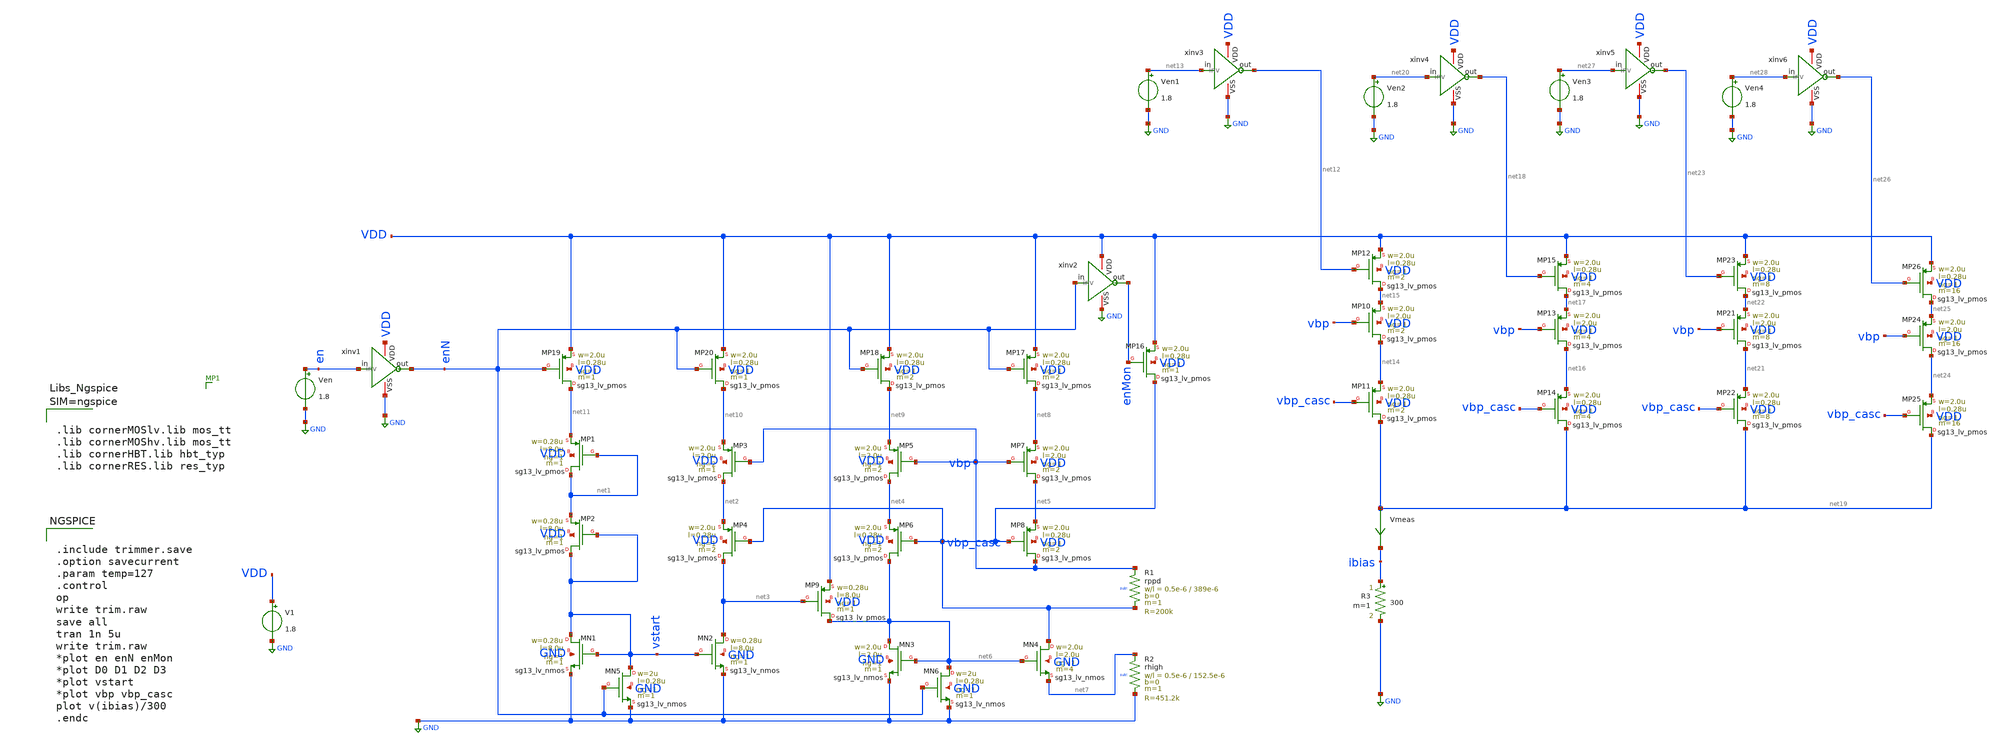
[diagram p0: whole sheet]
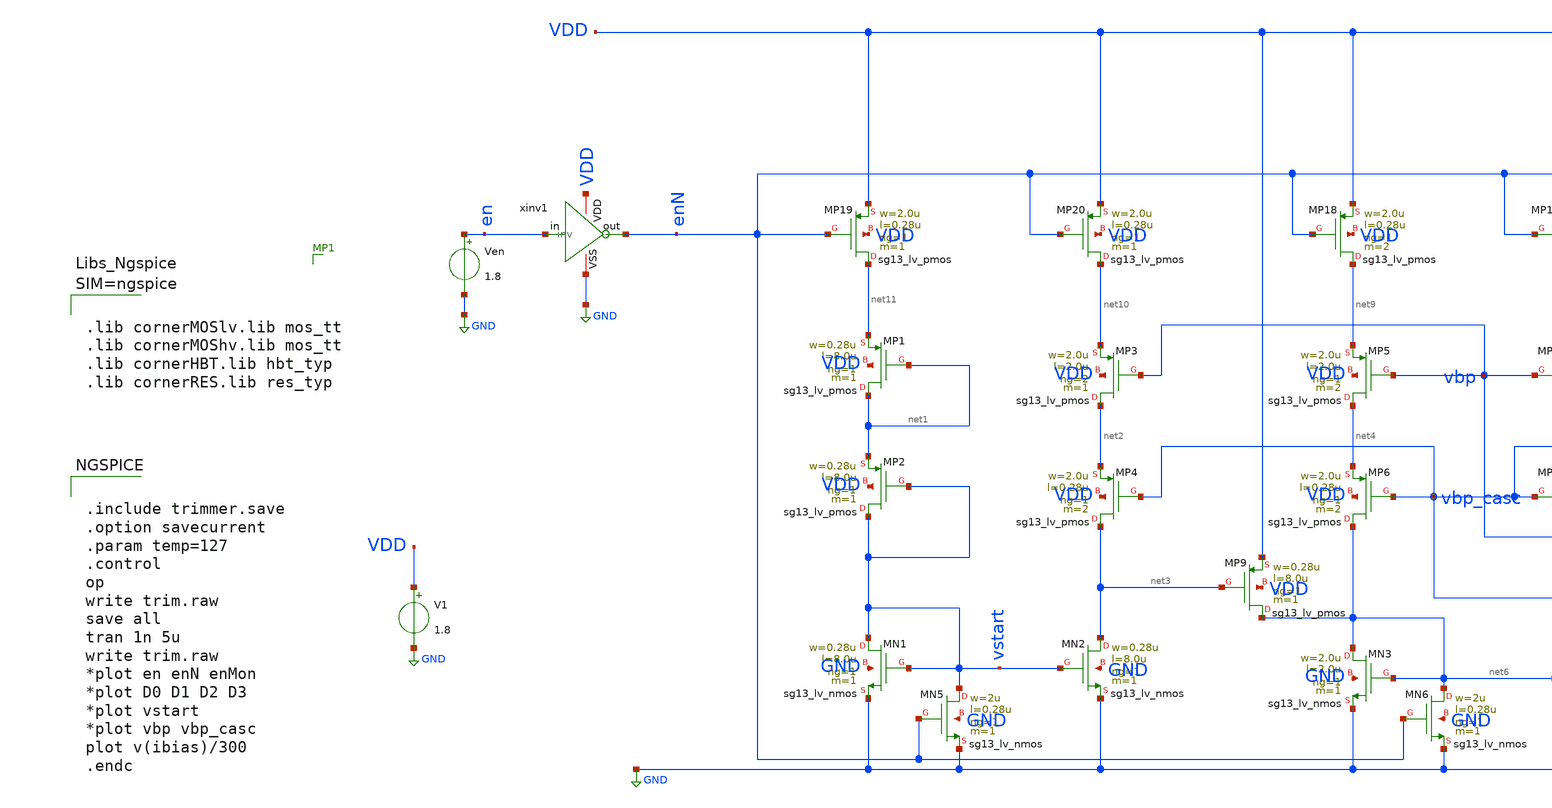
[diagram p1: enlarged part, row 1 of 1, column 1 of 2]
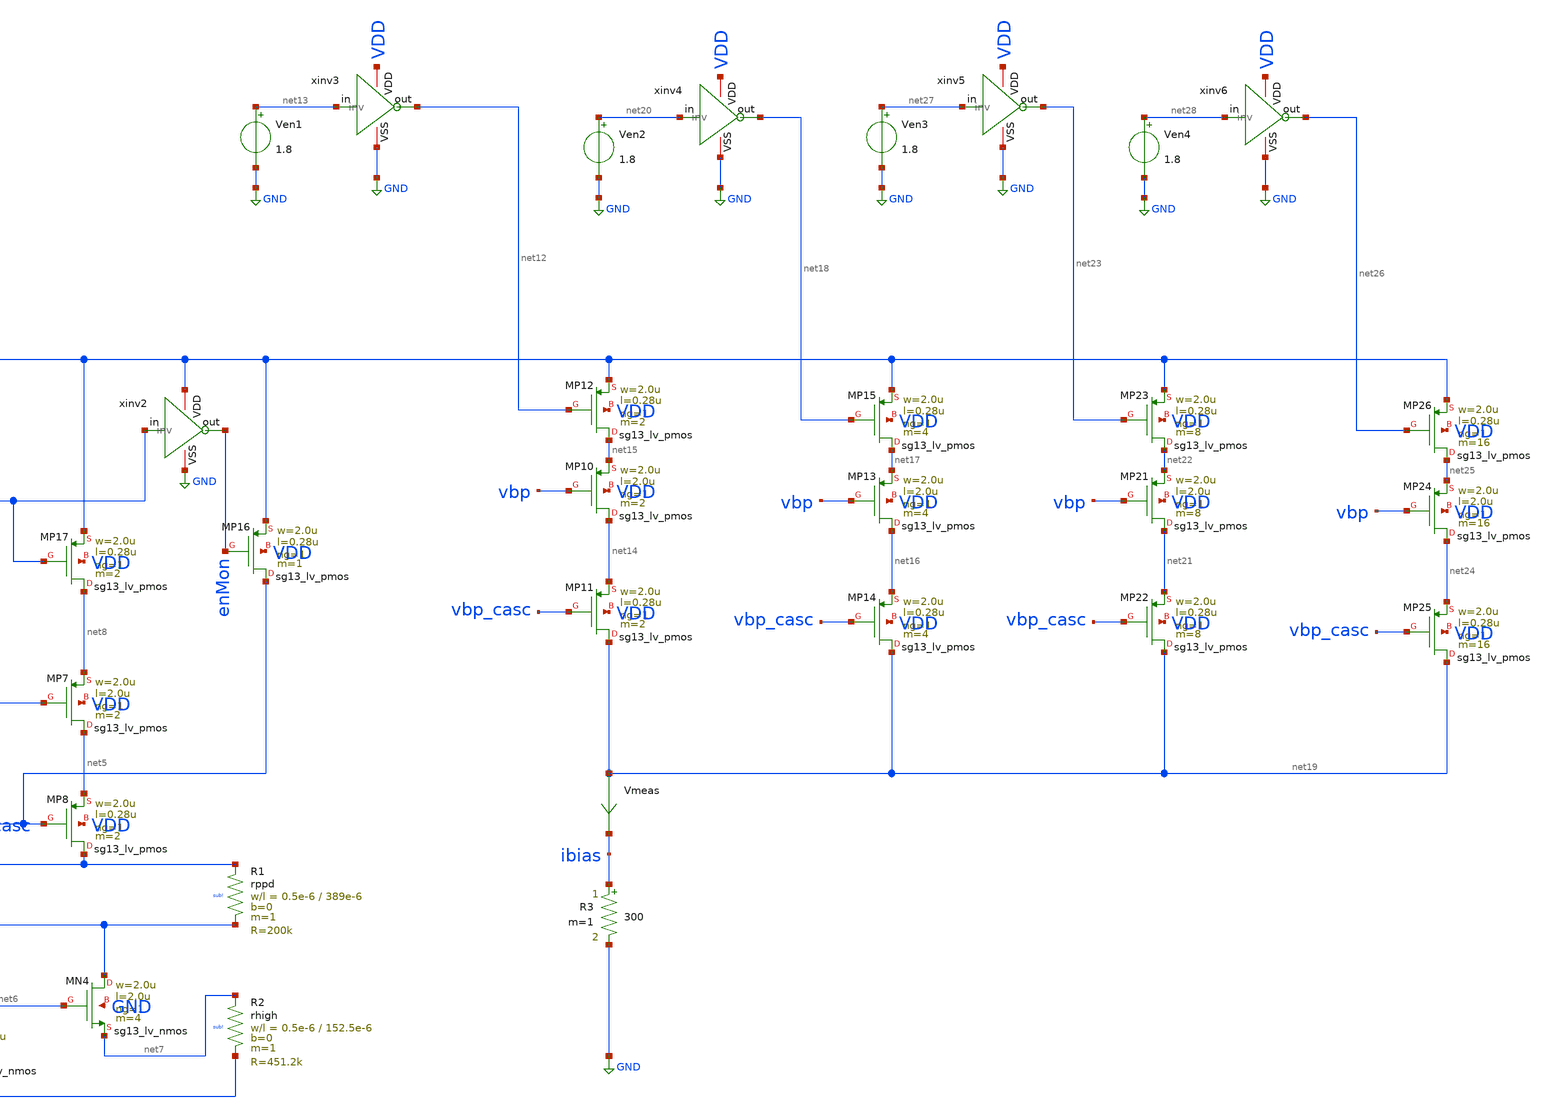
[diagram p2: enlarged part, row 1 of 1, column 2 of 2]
** sch_path: blocks/composite/dpi_adexp_neuron/design_data/xschem/dev/trimmer2_final.sch
**.subckt trimmer2_final
XMP1 net1 net1 net11 VDD sg13_lv_pmos w=0.28u l=8.0u ng=1 m=1 mm_ok=1
XMP2 vstart vstart net1 VDD sg13_lv_pmos w=0.28u l=8.0u ng=1 m=1 mm_ok=1
XMN2 net3 vstart GND GND sg13_lv_nmos w=0.28u l=8.0u ng=1 m=1 mm_ok=1
XMN1 vstart vstart GND GND sg13_lv_nmos w=0.28u l=8.0u ng=1 m=1 mm_ok=1
XMP3 net2 vbp net10 VDD sg13_lv_pmos w=2.0u l=2.0u ng=2 m=1 mm_ok=1
XMP4 net3 vbp_casc net2 VDD sg13_lv_pmos w=2.0u l=0.28u ng=1 m=2 mm_ok=1
XMP5 net4 vbp net9 VDD sg13_lv_pmos w=2.0u l=2.0u ng=1 m=2 mm_ok=1
XMP6 net6 vbp_casc net4 VDD sg13_lv_pmos w=2.0u l=0.28u ng=1 m=2 mm_ok=1
XMP7 net5 vbp net8 VDD sg13_lv_pmos w=2.0u l=2.0u ng=1 m=2 mm_ok=1
XMP8 vbp vbp_casc net5 VDD sg13_lv_pmos w=2.0u l=0.28u ng=1 m=2 mm_ok=1
XMP9 net6 net3 VDD VDD sg13_lv_pmos w=0.28u l=8.0u ng=1 m=1 mm_ok=1
XMN3 net6 net6 GND GND sg13_lv_nmos w=2.0u l=2.0u ng=1 m=1 mm_ok=1
XMN4 vbp_casc net6 net7 GND sg13_lv_nmos w=2.0u l=2.0u ng=1 m=4 mm_ok=1
XR1 vbp vbp_casc sub! rppd w=0.5e-6 l=389e-6 m=1 b=0 mm_ok=1
XR2 net7 GND sub! rhigh w=0.5e-6 l=152.5e-6 m=1 b=0 mm_ok=1
R3 ibias GND 300 m=1
XMP10 net14 vbp net15 VDD sg13_lv_pmos w=2.0u l=2.0u ng=1 m=2 mm_ok=1
XMP11 net19 vbp_casc net14 VDD sg13_lv_pmos w=2.0u l=0.28u ng=1 m=2 mm_ok=1
XMP16 vbp_casc enMon VDD VDD sg13_lv_pmos w=2.0u l=0.28u ng=1 m=1 mm_ok=1
XMP17 net8 enN VDD VDD sg13_lv_pmos w=2.0u l=0.28u ng=1 m=2 mm_ok=1
XMP18 net9 enN VDD VDD sg13_lv_pmos w=2.0u l=0.28u ng=1 m=2 mm_ok=1
XMP19 net11 enN VDD VDD sg13_lv_pmos w=2.0u l=0.28u ng=1 m=1 mm_ok=1
XMP20 net10 enN VDD VDD sg13_lv_pmos w=2.0u l=0.28u ng=1 m=1 mm_ok=1
XMN5 vstart enN GND GND sg13_lv_nmos w=2u l=0.28u ng=1 m=1 mm_ok=1
XMN6 net6 enN GND GND sg13_lv_nmos w=2u l=0.28u ng=1 m=1 mm_ok=1
V1 VDD GND 1.8
Ven en GND 1.8
xinv1 VDD en enN GND inv
xinv2 VDD enN enMon GND inv
XMP12 net15 net12 VDD VDD sg13_lv_pmos w=2.0u l=0.28u ng=1 m=2 mm_ok=1
Ven1 net13 GND 1.8
xinv3 VDD net13 net12 GND inv
XMP13 net16 vbp net17 VDD sg13_lv_pmos w=2.0u l=2.0u ng=1 m=4 mm_ok=1
XMP14 net19 vbp_casc net16 VDD sg13_lv_pmos w=2.0u l=0.28u ng=1 m=4 mm_ok=1
XMP15 net17 net18 VDD VDD sg13_lv_pmos w=2.0u l=0.28u ng=1 m=4 mm_ok=1
Ven2 net20 GND 1.8
xinv4 VDD net20 net18 GND inv
XMP21 net21 vbp net22 VDD sg13_lv_pmos w=2.0u l=2.0u ng=1 m=8 mm_ok=1
XMP22 net19 vbp_casc net21 VDD sg13_lv_pmos w=2.0u l=0.28u ng=1 m=8 mm_ok=1
XMP23 net22 net23 VDD VDD sg13_lv_pmos w=2.0u l=0.28u ng=1 m=8 mm_ok=1
XMP24 net24 vbp net25 VDD sg13_lv_pmos w=2.0u l=2.0u ng=1 m=16 mm_ok=1
XMP25 net19 vbp_casc net24 VDD sg13_lv_pmos w=2.0u l=0.28u ng=1 m=16 mm_ok=1
XMP26 net25 net26 VDD VDD sg13_lv_pmos w=2.0u l=0.28u ng=1 m=16 mm_ok=1
Ven3 net27 GND 1.8
xinv5 VDD net27 net23 GND inv
Ven4 net28 GND 1.8
xinv6 VDD net28 net26 GND inv
Vmeas net19 ibias 0
.save i(vmeas)
**** begin user architecture code


.include trimmer.save
.option savecurrent
.param temp=127
.control
op
write trim.raw
save all
tran 1n 5u
write trim.raw
*plot en enN enMon
*plot D0 D1 D2 D3
*plot vstart
*plot vbp vbp_casc
plot v(ibias)/300
.endc





.lib cornerMOSlv.lib mos_tt
.lib cornerMOShv.lib mos_tt
.lib cornerHBT.lib hbt_typ
.lib cornerRES.lib res_typ



**** end user architecture code
**.ends

* expanding   symbol:  inv.sym # of pins=4
** sym_path: blocks/composite/dpi_adexp_neuron/design_data/xschem/dev/inv.sym
** sch_path: blocks/composite/dpi_adexp_neuron/design_data/xschem/dev/inv.sch
.subckt inv VDD in out VSS
*.iopin VDD
*.ipin in
*.iopin VSS
*.opin out
XM1 out in VSS VSS sg13_lv_nmos w=2.0u l=0.28u ng=1 m=1 mm_ok=1
XM2 out in VDD VDD sg13_lv_pmos w=2.0u l=0.28u ng=1 m=1 mm_ok=1
.ends

.GLOBAL GND
.end
